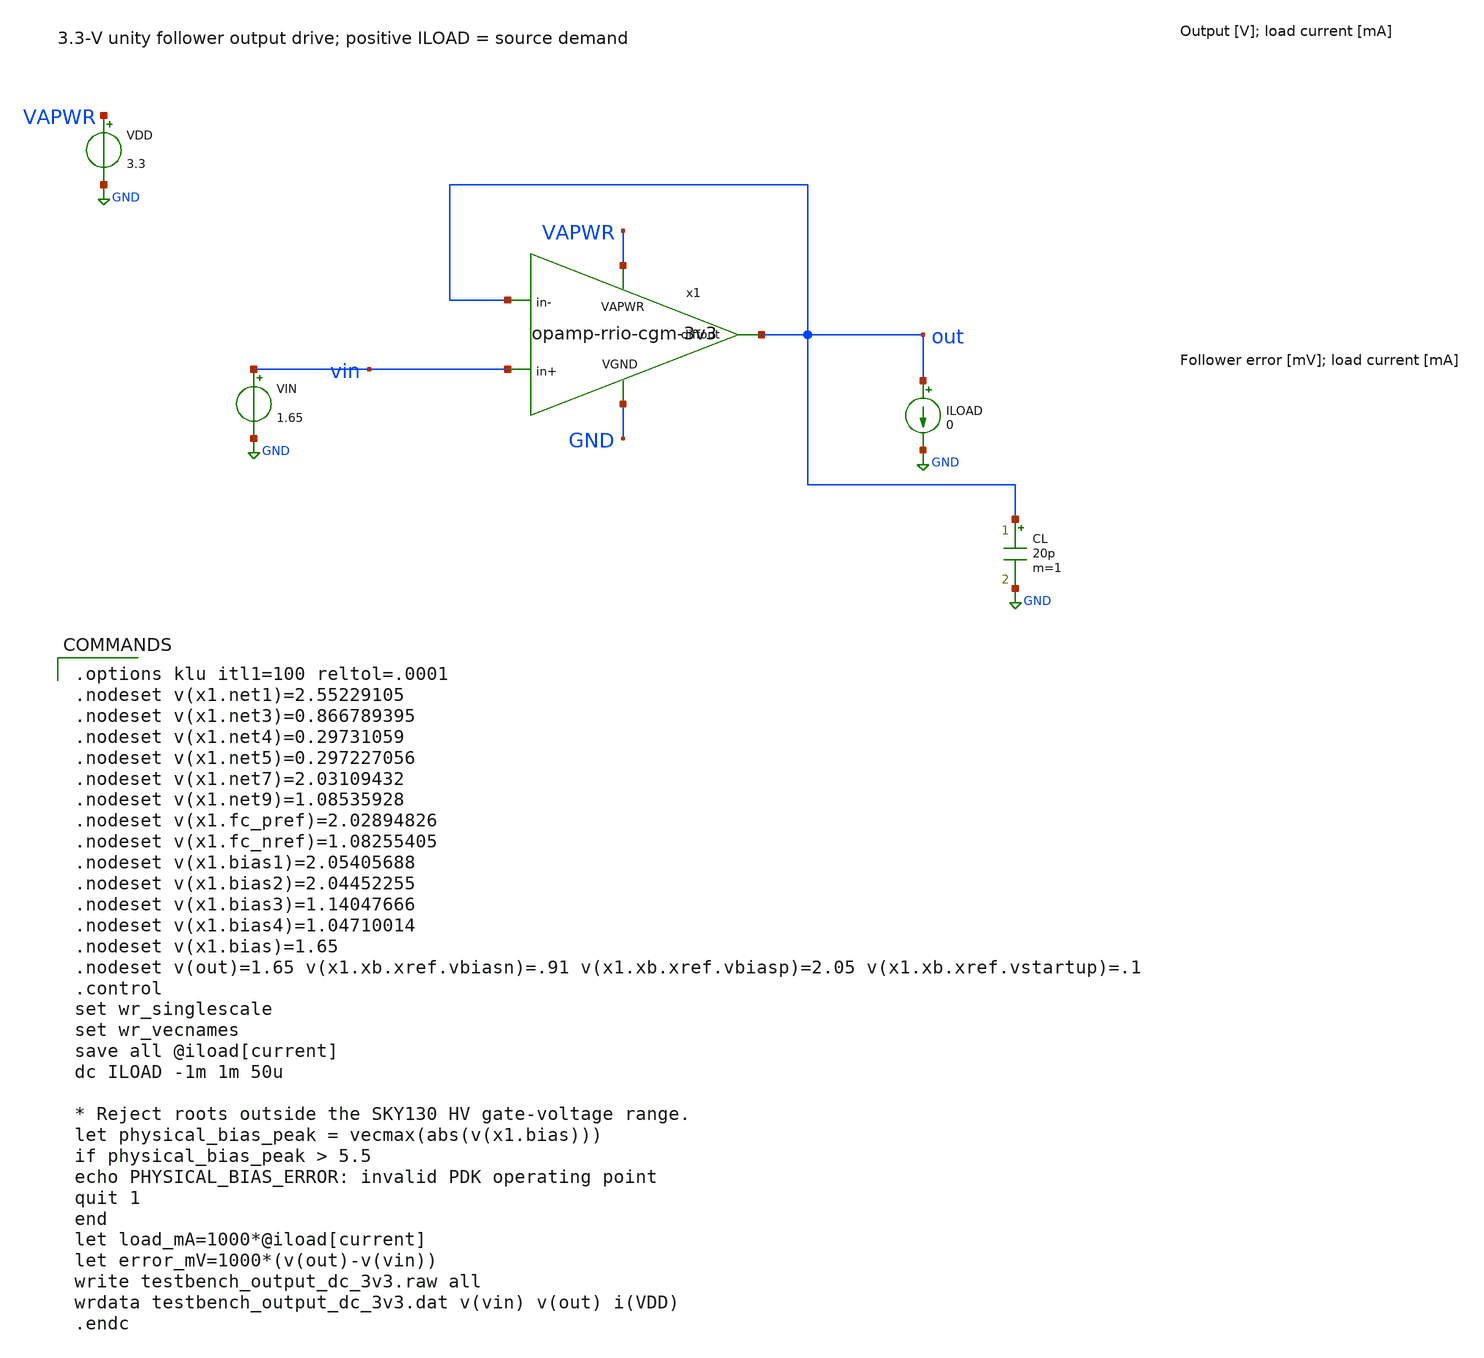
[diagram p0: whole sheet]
** sch_path: xschem/testbench_output_dc_3v3.sch
**.subckt testbench_output_dc_3v3
x1 VAPWR out vin out GND opamp-rrio-cgm-3v3
VDD VAPWR GND 3.3
VIN vin GND 1.65
ILOAD out GND 0
CL out GND 20p m=1
**** begin user architecture code
 .lib $::SKYWATER_MODELS/sky130.lib.spice tt

.options klu itl1=100 reltol=.0001
.nodeset v(x1.net1)=2.55229105
.nodeset v(x1.net3)=0.866789395
.nodeset v(x1.net4)=0.29731059
.nodeset v(x1.net5)=0.297227056
.nodeset v(x1.net7)=2.03109432
.nodeset v(x1.net9)=1.08535928
.nodeset v(x1.fc_pref)=2.02894826
.nodeset v(x1.fc_nref)=1.08255405
.nodeset v(x1.bias1)=2.05405688
.nodeset v(x1.bias2)=2.04452255
.nodeset v(x1.bias3)=1.14047666
.nodeset v(x1.bias4)=1.04710014
.nodeset v(x1.bias)=1.65
.nodeset v(out)=1.65 v(x1.xb.xref.vbiasn)=.91 v(x1.xb.xref.vbiasp)=2.05 v(x1.xb.xref.vstartup)=.1
.control
set wr_singlescale
set wr_vecnames
save all @iload[current]
dc ILOAD -1m 1m 50u

* Reject roots outside the SKY130 HV gate-voltage range.
let physical_bias_peak = vecmax(abs(v(x1.bias)))
if physical_bias_peak > 5.5
echo PHYSICAL_BIAS_ERROR: invalid PDK operating point
quit 1
end
let load_mA=1000*@iload[current]
let error_mV=1000*(v(out)-v(vin))
write testbench_output_dc_3v3.raw all
wrdata testbench_output_dc_3v3.dat v(vin) v(out) i(VDD)
.endc

**** end user architecture code
**.ends
.GLOBAL GND
.end
